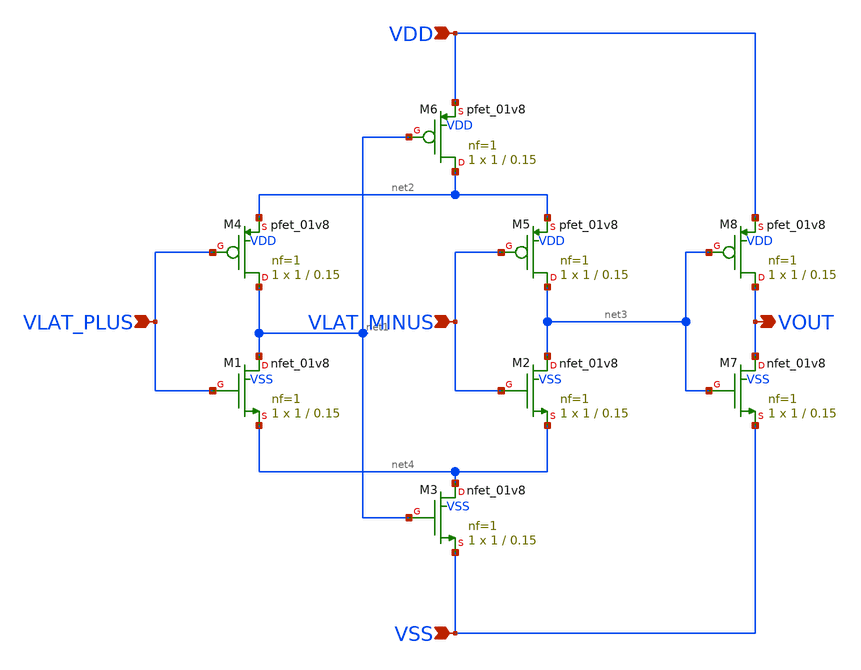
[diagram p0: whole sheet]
** sch_path: xschem/flash_converter/post_amplifier.sch
**.subckt post_amplifier VLAT_PLUS VLAT_MINUS VDD VSS VOUT
*.ipin VLAT_PLUS
*.ipin VLAT_MINUS
*.ipin VDD
*.ipin VSS
*.opin VOUT
XM1 net1 VLAT_PLUS net4 VSS sky130_fd_pr__nfet_01v8 L=0.15 W=1 nf=1 ad='int((nf+1)/2) * W/nf * 0.29'
+ as='int((nf+2)/2) * W/nf * 0.29' pd='2*int((nf+1)/2) * (W/nf + 0.29)' ps='2*int((nf+2)/2) * (W/nf + 0.29)'
+ nrd='0.29 / W' nrs='0.29 / W' sa=0 sb=0 sd=0 mult=1 m=1
XM2 net3 VLAT_MINUS net4 VSS sky130_fd_pr__nfet_01v8 L=0.15 W=1 nf=1 ad='int((nf+1)/2) * W/nf * 0.29'
+ as='int((nf+2)/2) * W/nf * 0.29' pd='2*int((nf+1)/2) * (W/nf + 0.29)' ps='2*int((nf+2)/2) * (W/nf + 0.29)'
+ nrd='0.29 / W' nrs='0.29 / W' sa=0 sb=0 sd=0 mult=1 m=1
XM3 net4 net1 VSS VSS sky130_fd_pr__nfet_01v8 L=0.15 W=1 nf=1 ad='int((nf+1)/2) * W/nf * 0.29' as='int((nf+2)/2) * W/nf * 0.29'
+ pd='2*int((nf+1)/2) * (W/nf + 0.29)' ps='2*int((nf+2)/2) * (W/nf + 0.29)' nrd='0.29 / W' nrs='0.29 / W'
+ sa=0 sb=0 sd=0 mult=1 m=1
XM4 net1 VLAT_PLUS net2 VDD sky130_fd_pr__pfet_01v8 L=0.15 W=1 nf=1 ad='int((nf+1)/2) * W/nf * 0.29'
+ as='int((nf+2)/2) * W/nf * 0.29' pd='2*int((nf+1)/2) * (W/nf + 0.29)' ps='2*int((nf+2)/2) * (W/nf + 0.29)'
+ nrd='0.29 / W' nrs='0.29 / W' sa=0 sb=0 sd=0 mult=1 m=1
XM5 net3 VLAT_MINUS net2 VDD sky130_fd_pr__pfet_01v8 L=0.15 W=1 nf=1 ad='int((nf+1)/2) * W/nf * 0.29'
+ as='int((nf+2)/2) * W/nf * 0.29' pd='2*int((nf+1)/2) * (W/nf + 0.29)' ps='2*int((nf+2)/2) * (W/nf + 0.29)'
+ nrd='0.29 / W' nrs='0.29 / W' sa=0 sb=0 sd=0 mult=1 m=1
XM6 net2 net1 VDD VDD sky130_fd_pr__pfet_01v8 L=0.15 W=1 nf=1 ad='int((nf+1)/2) * W/nf * 0.29' as='int((nf+2)/2) * W/nf * 0.29'
+ pd='2*int((nf+1)/2) * (W/nf + 0.29)' ps='2*int((nf+2)/2) * (W/nf + 0.29)' nrd='0.29 / W' nrs='0.29 / W'
+ sa=0 sb=0 sd=0 mult=1 m=1
XM7 VOUT net3 VSS VSS sky130_fd_pr__nfet_01v8 L=0.15 W=1 nf=1 ad='int((nf+1)/2) * W/nf * 0.29' as='int((nf+2)/2) * W/nf * 0.29'
+ pd='2*int((nf+1)/2) * (W/nf + 0.29)' ps='2*int((nf+2)/2) * (W/nf + 0.29)' nrd='0.29 / W' nrs='0.29 / W'
+ sa=0 sb=0 sd=0 mult=1 m=1
XM8 VOUT net3 VDD VDD sky130_fd_pr__pfet_01v8 L=0.15 W=1 nf=1 ad='int((nf+1)/2) * W/nf * 0.29' as='int((nf+2)/2) * W/nf * 0.29'
+ pd='2*int((nf+1)/2) * (W/nf + 0.29)' ps='2*int((nf+2)/2) * (W/nf + 0.29)' nrd='0.29 / W' nrs='0.29 / W'
+ sa=0 sb=0 sd=0 mult=1 m=1
**.ends
.end
